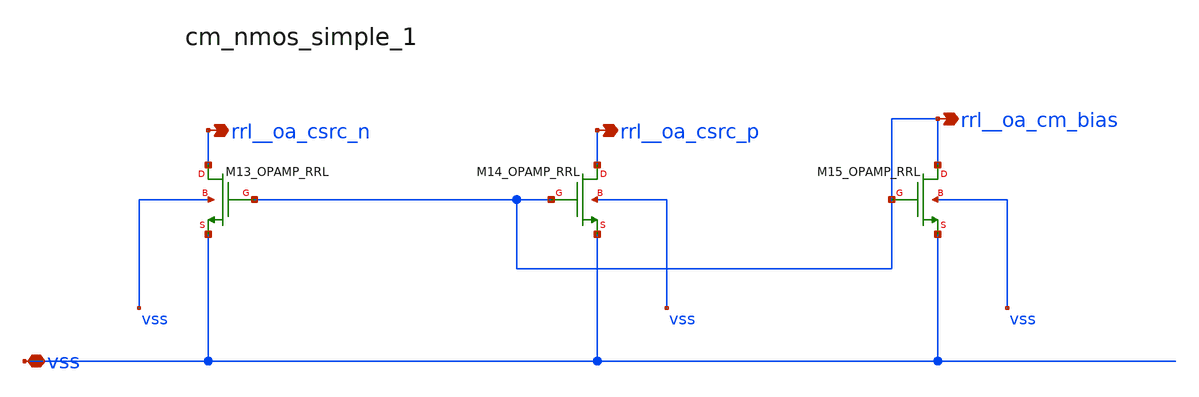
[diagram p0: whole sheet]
** sch_path: analog-db/raw/ia_004_fan_chopper_rrl/hier/blocks/cm_nmos_simple_1.sch
**.subckt cm_nmos_simple_1 vss rrl__oa_csrc_n rrl__oa_csrc_p rrl__oa_cm_bias
*.iopin vss
*.opin rrl__oa_csrc_n
*.opin rrl__oa_csrc_p
*.opin rrl__oa_cm_bias
XM13_OPAMP_RRL rrl__oa_csrc_n rrl__oa_cm_bias vss vss sg13_lv_nmos w=x_dut_xm13_opamp_rrl_w
+ l=x_dut_xm13_opamp_rrl_l ng=1 m=x_dut_xm13_opamp_rrl_m
XM14_OPAMP_RRL rrl__oa_csrc_p rrl__oa_cm_bias vss vss sg13_lv_nmos w=x_dut_xm14_opamp_rrl_w
+ l=x_dut_xm14_opamp_rrl_l ng=1 m=x_dut_xm14_opamp_rrl_m
XM15_OPAMP_RRL rrl__oa_cm_bias rrl__oa_cm_bias vss vss sg13_lv_nmos w=x_dut_xm15_opamp_rrl_w
+ l=x_dut_xm15_opamp_rrl_l ng=1 m=x_dut_xm15_opamp_rrl_m
**.ends
.end
